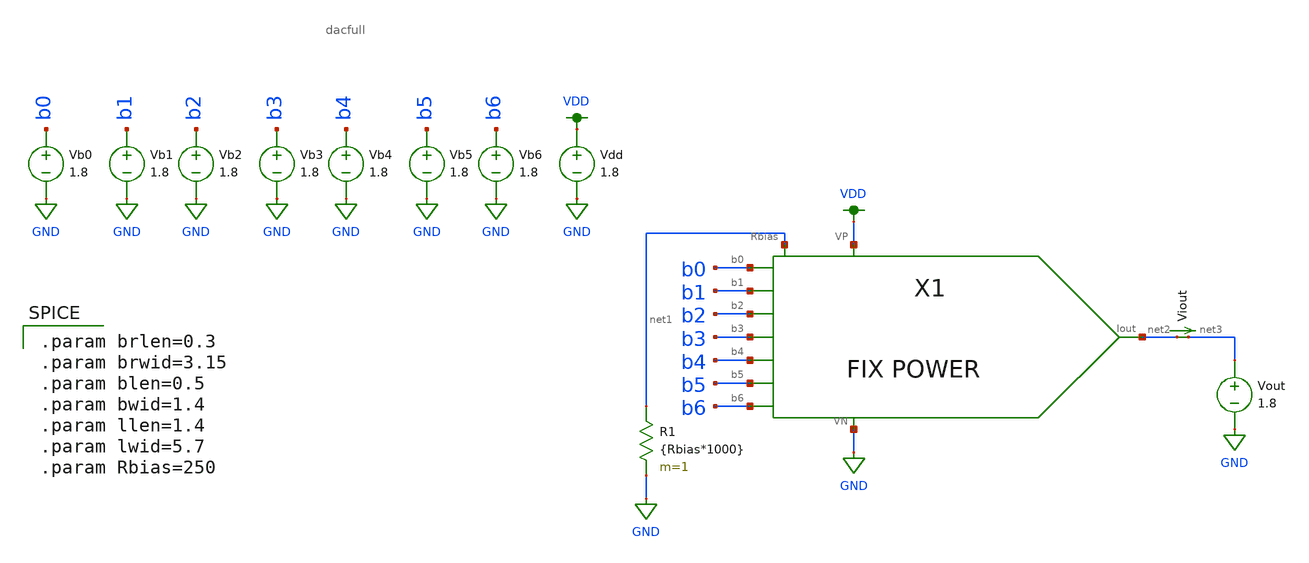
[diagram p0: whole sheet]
** sch_path: design-files/improved/dac_harness-m2.sch
**.subckt dac_harness-m2
X1 VDD b0 b1 b2 b3 b4 b5 b6 GND net2 net1 dacfull
Vb0 b0 GND 1.8
Vb1 b1 GND 1.8
Vb2 b2 GND 1.8
Vb3 b3 GND 1.8
Vb4 b4 GND 1.8
Vb5 b5 GND 1.8
Vb6 b6 GND 1.8
Vdd VDD GND 1.8
R1 net1 GND {Rbias*1000} m=1
Viout net2 net3 0
.save i(viout)
Vout net3 GND 1.8
**** begin user architecture code


.control
	set wr_vecnames
	set wr_singlescale
	let code = 0
	while code < 128
		if code eq 0
			let nb0 = 0
		else
			let nb0 = (code % 2)*1.8
		end
		if floor(code / 2) eq 0
			let nb1 = 0
		else
			let nb1 = (floor(code / 2) % 2)*1.8
		end
		if floor(code / 4) eq 0
			let nb2 = 0
		else
			let nb2 = (floor(code / 4) % 2)*1.8
		end
		if floor(code / 8) eq 0
			let nb3 = 0
		else
			let nb3 = (floor(code / 8) % 2)*1.8
		end
		if floor(code / 16) eq 0
			let nb4 = 0
		else
			let nb4 = (floor(code / 16) % 2)*1.8
		end
		if floor(code / 32) eq 0
			let nb5 = 0
		else
			let nb5 = (floor(code / 32) % 2)*1.8
		end
		if floor(code / 64) eq 0
			let nb6 = 0
		else
			let nb6 = (floor(code / 64) % 2)*1.8
		end
		alter Vb0 $&nb0
		alter Vb1 $&nb1
		alter Vb2 $&nb2
		alter Vb3 $&nb3
		alter Vb4 $&nb4
		alter Vb5 $&nb5
		alter Vb6 $&nb6
		save i(Viout) v(b0) v(b1) v(b2) v(b3) v(b4) v(b5) v(b6)
		op
		wrdata ~/VLSI/VLSI-MP4/design-files/improved/dacdata.txt i(Viout)
		if code eq 0
			set appendwrite
			set wr_vecnames = FALSE
		end
		let code = code + 1
	end
	quit
.endc


.option wnflag=1
.param MC_SWITCH=0
.lib ~/skywater/skywater-pdk/libraries/sky130_fd_pr_ngspice/latest/models/sky130.lib.spice tt


.param brlen=0.3
.param brwid=3.15
.param blen=0.5
.param bwid=1.4
.param llen=1.4
.param lwid=5.7
.param Rbias=250

**** end user architecture code
**.ends
.GLOBAL GND
.GLOBAL VDD
.end
